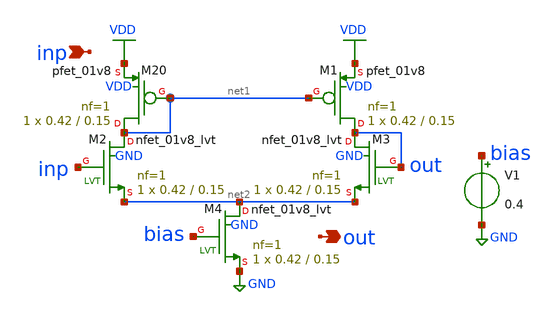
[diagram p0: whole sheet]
** sch_path: xschem/tryandtest/unitygainbuffer.sch
**.subckt unitygainbuffer out inp
*.opin out
*.ipin inp
XM20 net1 net1 VDD VDD sky130_fd_pr__pfet_01v8 L=0.15 W=0.42 nf=1 ad='int((nf+1)/2) * W/nf * 0.29' as='int((nf+2)/2) * W/nf * 0.29'
+ pd='2*int((nf+1)/2) * (W/nf + 0.29)' ps='2*int((nf+2)/2) * (W/nf + 0.29)' nrd='0.29 / W' nrs='0.29 / W'
+ sa=0 sb=0 sd=0 mult=1 m=1
XM1 out net1 VDD VDD sky130_fd_pr__pfet_01v8 L=0.15 W=0.42 nf=1 ad='int((nf+1)/2) * W/nf * 0.29' as='int((nf+2)/2) * W/nf * 0.29'
+ pd='2*int((nf+1)/2) * (W/nf + 0.29)' ps='2*int((nf+2)/2) * (W/nf + 0.29)' nrd='0.29 / W' nrs='0.29 / W'
+ sa=0 sb=0 sd=0 mult=1 m=1
XM2 net1 inp net2 GND sky130_fd_pr__nfet_01v8_lvt L=0.15 W=0.42 nf=1 ad='int((nf+1)/2) * W/nf * 0.29'
+ as='int((nf+2)/2) * W/nf * 0.29' pd='2*int((nf+1)/2) * (W/nf + 0.29)' ps='2*int((nf+2)/2) * (W/nf + 0.29)'
+ nrd='0.29 / W' nrs='0.29 / W' sa=0 sb=0 sd=0 mult=1 m=1
XM3 out out net2 GND sky130_fd_pr__nfet_01v8_lvt L=0.15 W=0.42 nf=1 ad='int((nf+1)/2) * W/nf * 0.29'
+ as='int((nf+2)/2) * W/nf * 0.29' pd='2*int((nf+1)/2) * (W/nf + 0.29)' ps='2*int((nf+2)/2) * (W/nf + 0.29)'
+ nrd='0.29 / W' nrs='0.29 / W' sa=0 sb=0 sd=0 mult=1 m=1
V1 bias GND 0.4
XM4 net2 bias GND GND sky130_fd_pr__nfet_01v8_lvt L=0.15 W=0.42 nf=1 ad='int((nf+1)/2) * W/nf * 0.29'
+ as='int((nf+2)/2) * W/nf * 0.29' pd='2*int((nf+1)/2) * (W/nf + 0.29)' ps='2*int((nf+2)/2) * (W/nf + 0.29)'
+ nrd='0.29 / W' nrs='0.29 / W' sa=0 sb=0 sd=0 mult=1 m=1
**.ends
.GLOBAL GND
.GLOBAL VDD
.end
